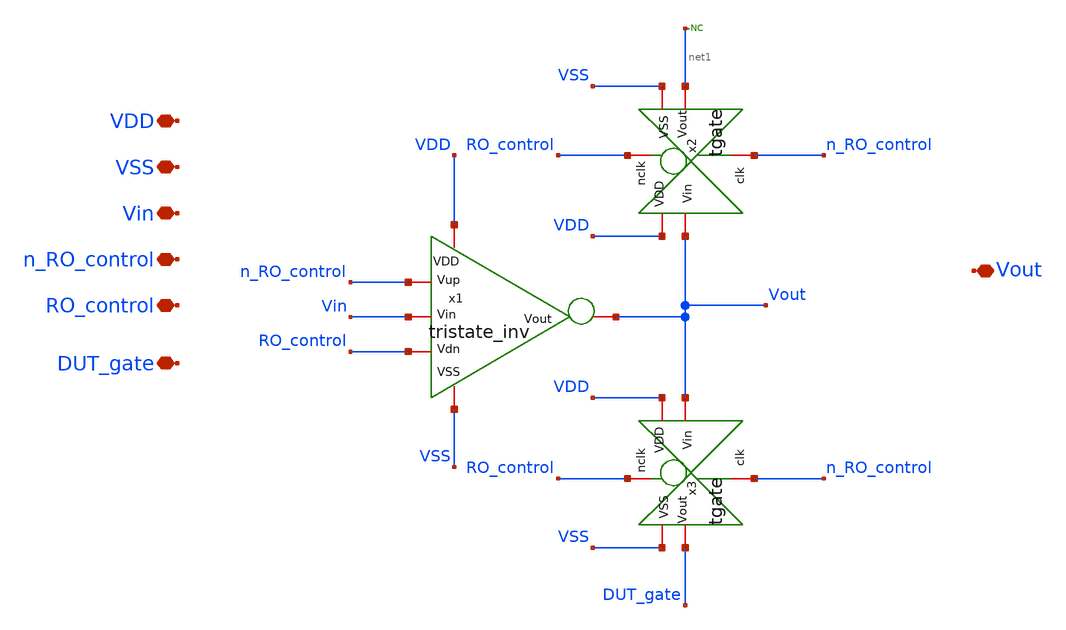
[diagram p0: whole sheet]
** sch_path: TT/rovcel3.sch
**.subckt rovcel3 VDD VSS Vin n_RO_control RO_control DUT_gate Vout
*.iopin VDD
*.iopin VSS
*.iopin Vin
*.iopin n_RO_control
*.iopin RO_control
*.iopin DUT_gate
*.iopin Vout
x1 VDD VSS Vin n_RO_control RO_control Vout tristate_inv
x2 RO_control VDD Vout net1 VSS n_RO_control tgate
x3 RO_control VDD Vout DUT_gate VSS n_RO_control tgate
* noconn #net1
**.ends

* expanding   symbol:  /foss/designs/Projects/RO_reliability/xschem/tristate_inv.sym # of pins=6
** sym_path: TT/tristate_inv.sym
** sch_path: TT/tristate_inv.sch
.subckt tristate_inv VDD VSS Vin Vup Vdn Vout
*.iopin VDD
*.iopin VSS
*.iopin Vin
*.iopin Vout
*.iopin Vup
*.iopin Vdn
XM1 net1 Vup VDD VDD sky130_fd_pr__pfet_01v8 L=0.15 W=4.75 nf=1 ad='int((nf+1)/2) * W/nf * 0.29' as='int((nf+2)/2) * W/nf * 0.29'
+ pd='2*int((nf+1)/2) * (W/nf + 0.29)' ps='2*int((nf+2)/2) * (W/nf + 0.29)' nrd='0.29 / W' nrs='0.29 / W'
+ sa=0 sb=0 sd=0 mult=40 m=40
XM2 Vout Vin net1 VDD sky130_fd_pr__pfet_01v8 L=0.15 W=4.75 nf=1 ad='int((nf+1)/2) * W/nf * 0.29' as='int((nf+2)/2) * W/nf * 0.29'
+ pd='2*int((nf+1)/2) * (W/nf + 0.29)' ps='2*int((nf+2)/2) * (W/nf + 0.29)' nrd='0.29 / W' nrs='0.29 / W'
+ sa=0 sb=0 sd=0 mult=4 m=4
XM3 Vout Vin net2 VSS sky130_fd_pr__nfet_01v8 L=0.15 W=2.1 nf=1 ad='int((nf+1)/2) * W/nf * 0.29' as='int((nf+2)/2) * W/nf * 0.29'
+ pd='2*int((nf+1)/2) * (W/nf + 0.29)' ps='2*int((nf+2)/2) * (W/nf + 0.29)' nrd='0.29 / W' nrs='0.29 / W'
+ sa=0 sb=0 sd=0 mult=2 m=2
XM4 net2 Vdn VSS VSS sky130_fd_pr__nfet_01v8 L=0.15 W=2.1 nf=1 ad='int((nf+1)/2) * W/nf * 0.29' as='int((nf+2)/2) * W/nf * 0.29'
+ pd='2*int((nf+1)/2) * (W/nf + 0.29)' ps='2*int((nf+2)/2) * (W/nf + 0.29)' nrd='0.29 / W' nrs='0.29 / W'
+ sa=0 sb=0 sd=0 mult=20 m=20
.ends


* expanding   symbol:  /foss/designs/Projects/RO_reliability/xschem/tgate.sym # of pins=6
** sym_path: TT/tgate.sym
** sch_path: TT/tgate.sch
.subckt tgate nclk VDD Vin Vout VSS clk
*.iopin nclk
*.iopin clk
*.iopin VDD
*.iopin VSS
*.iopin Vout
*.iopin Vin
XM1 Vin nclk Vout VDD sky130_fd_pr__pfet_01v8 L=0.15 W=0.45 nf=1 ad='int((nf+1)/2) * W/nf * 0.29' as='int((nf+2)/2) * W/nf * 0.29'
+ pd='2*int((nf+1)/2) * (W/nf + 0.29)' ps='2*int((nf+2)/2) * (W/nf + 0.29)' nrd='0.29 / W' nrs='0.29 / W'
+ sa=0 sb=0 sd=0 mult=1 m=1
XM2 Vin clk Vout VSS sky130_fd_pr__nfet_01v8 L=0.15 W=0.45 nf=1 ad='int((nf+1)/2) * W/nf * 0.29' as='int((nf+2)/2) * W/nf * 0.29'
+ pd='2*int((nf+1)/2) * (W/nf + 0.29)' ps='2*int((nf+2)/2) * (W/nf + 0.29)' nrd='0.29 / W' nrs='0.29 / W'
+ sa=0 sb=0 sd=0 mult=1 m=1
.ends

.end
